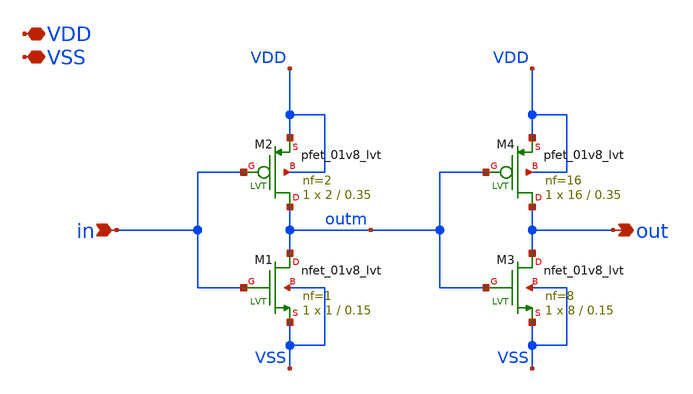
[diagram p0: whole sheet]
** sch_path: xschem/Utili/buffer.sch
**.subckt buffer VDD VSS in out
*.iopin VDD
*.iopin VSS
*.ipin in
*.opin out
XM1 outm in VSS VSS sky130_fd_pr__nfet_01v8_lvt L=0.15 W=1 nf=1 ad='int((nf+1)/2) * W/nf * 0.29' as='int((nf+2)/2) * W/nf * 0.29'
+ pd='2*int((nf+1)/2) * (W/nf + 0.29)' ps='2*int((nf+2)/2) * (W/nf + 0.29)' nrd='0.29 / W' nrs='0.29 / W'
+ sa=0 sb=0 sd=0 mult=1 m=1
XM2 outm in VDD VDD sky130_fd_pr__pfet_01v8_lvt L=0.35 W=2 nf=2 ad='int((nf+1)/2) * W/nf * 0.29' as='int((nf+2)/2) * W/nf * 0.29'
+ pd='2*int((nf+1)/2) * (W/nf + 0.29)' ps='2*int((nf+2)/2) * (W/nf + 0.29)' nrd='0.29 / W' nrs='0.29 / W'
+ sa=0 sb=0 sd=0 mult=1 m=1
XM3 out outm VSS VSS sky130_fd_pr__nfet_01v8_lvt L=0.15 W=8 nf=8 ad='int((nf+1)/2) * W/nf * 0.29' as='int((nf+2)/2) * W/nf * 0.29'
+ pd='2*int((nf+1)/2) * (W/nf + 0.29)' ps='2*int((nf+2)/2) * (W/nf + 0.29)' nrd='0.29 / W' nrs='0.29 / W'
+ sa=0 sb=0 sd=0 mult=1 m=1
XM4 out outm VDD VDD sky130_fd_pr__pfet_01v8_lvt L=0.35 W=16 nf=16 ad='int((nf+1)/2) * W/nf * 0.29' as='int((nf+2)/2) * W/nf * 0.29'
+ pd='2*int((nf+1)/2) * (W/nf + 0.29)' ps='2*int((nf+2)/2) * (W/nf + 0.29)' nrd='0.29 / W' nrs='0.29 / W'
+ sa=0 sb=0 sd=0 mult=1 m=1
**.ends
.end
